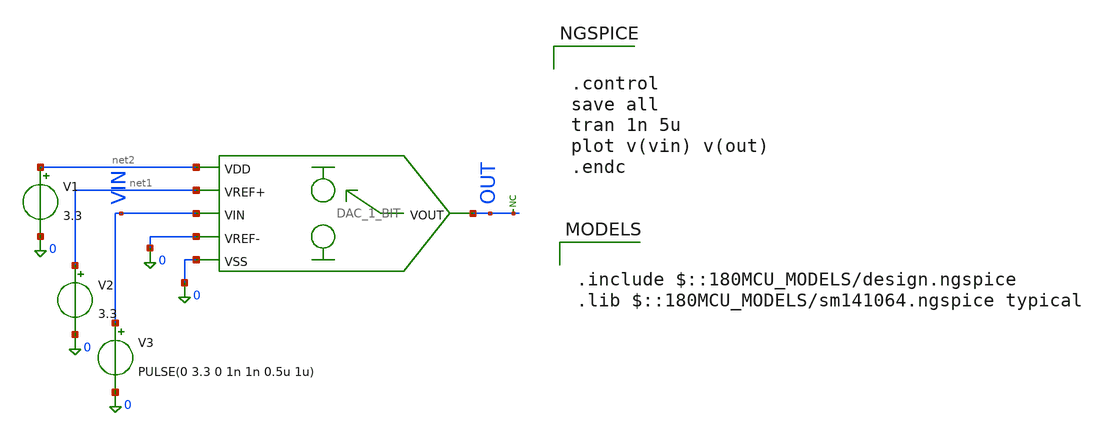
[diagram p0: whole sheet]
** sch_path: src/schematics/DAC 1 BIT/DAC_1_BIT_TB.sch
**.subckt DAC_1_BIT_TB
V1 net2 0 3.3
V2 net1 0 3.3
V3 VIN 0 PULSE(0 3.3 0 1n 1n 0.5u 1u)
* noconn OUT
x1 net2 net1 VIN OUT 0 0 DAC_1_BIT
**** begin user architecture code


.control
save all
tran 1n 5u
plot v(vin) v(out)
.endc




.include $::180MCU_MODELS/design.ngspice
.lib $::180MCU_MODELS/sm141064.ngspice typical

**** end user architecture code
**.ends

* expanding   symbol:  DAC_1_BIT.sym # of pins=6
** sym_path: src/schematics/DAC 1 BIT/DAC_1_BIT.sym
** sch_path: src/schematics/DAC 1 BIT/DAC_1_BIT.sch
.subckt DAC_1_BIT VDD VREF+ VIN VOUT VREF- VSS
*.ipin VIN
*.ipin VREF+
*.ipin VREF-
*.opin VOUT
*.ipin VDD
*.ipin VSS
XM1 VOUT net1 VREF+ VSS nfet_03v3 L=0.28u W=6u nf=2 ad='int((nf+1)/2) * W/nf * 0.18u' as='int((nf+2)/2) * W/nf * 0.18u'
+ pd='2*int((nf+1)/2) * (W/nf + 0.18u)' ps='2*int((nf+2)/2) * (W/nf + 0.18u)' nrd='0.18u / W' nrs='0.18u / W'
+ sa=0 sb=0 sd=0 m=1
XM2 VOUT VIN VREF+ VDD pfet_03v3 L=0.28u W=6u nf=2 ad='int((nf+1)/2) * W/nf * 0.18u' as='int((nf+2)/2) * W/nf * 0.18u'
+ pd='2*int((nf+1)/2) * (W/nf + 0.18u)' ps='2*int((nf+2)/2) * (W/nf + 0.18u)' nrd='0.18u / W' nrs='0.18u / W'
+ sa=0 sb=0 sd=0 m=1
XM3 VOUT VIN VREF- VSS nfet_03v3 L=0.28u W=6u nf=2 ad='int((nf+1)/2) * W/nf * 0.18u' as='int((nf+2)/2) * W/nf * 0.18u'
+ pd='2*int((nf+1)/2) * (W/nf + 0.18u)' ps='2*int((nf+2)/2) * (W/nf + 0.18u)' nrd='0.18u / W' nrs='0.18u / W'
+ sa=0 sb=0 sd=0 m=1
XM4 VOUT net1 VREF- VDD pfet_03v3 L=0.28u W=6u nf=2 ad='int((nf+1)/2) * W/nf * 0.18u' as='int((nf+2)/2) * W/nf * 0.18u'
+ pd='2*int((nf+1)/2) * (W/nf + 0.18u)' ps='2*int((nf+2)/2) * (W/nf + 0.18u)' nrd='0.18u / W' nrs='0.18u / W'
+ sa=0 sb=0 sd=0 m=1
XM5 net1 VIN VDD VDD pfet_03v3 L=0.5u W=3u nf=1 ad='int((nf+1)/2) * W/nf * 0.18u' as='int((nf+2)/2) * W/nf * 0.18u'
+ pd='2*int((nf+1)/2) * (W/nf + 0.18u)' ps='2*int((nf+2)/2) * (W/nf + 0.18u)' nrd='0.18u / W' nrs='0.18u / W'
+ sa=0 sb=0 sd=0 m=1
XM6 net1 VIN VSS VSS nfet_03v3 L=0.5u W=3u nf=1 ad='int((nf+1)/2) * W/nf * 0.18u' as='int((nf+2)/2) * W/nf * 0.18u'
+ pd='2*int((nf+1)/2) * (W/nf + 0.18u)' ps='2*int((nf+2)/2) * (W/nf + 0.18u)' nrd='0.18u / W' nrs='0.18u / W'
+ sa=0 sb=0 sd=0 m=1
.ends

.end
